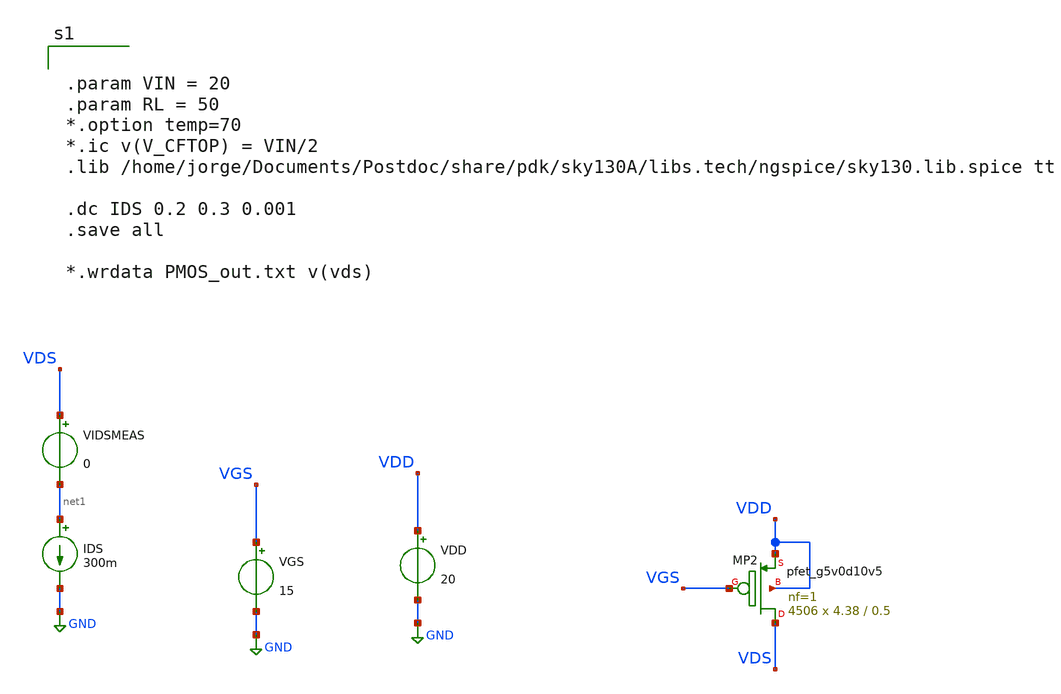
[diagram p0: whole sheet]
** sch_path: xschem/dev_switches/PMOS_allfingers_RONcalc_v2p1_20220623.sch
**.subckt PMOS_allfingers_RONcalc_v2p1_20220623
VGS VGS GND 15
IDS net1 GND 300m
VIDSMEAS VDS net1 0
XMP2 VDS VGS VDD VDD sky130_fd_pr__pfet_g5v0d10v5 L=0.5 W=4.38 nf=1 ad='int((nf+1)/2) * W/nf * 0.29'
+ as='int((nf+2)/2) * W/nf * 0.29' pd='2*int((nf+1)/2) * (W/nf + 0.29)' ps='2*int((nf+2)/2) * (W/nf + 0.29)'
+ nrd='0.29 / W' nrs='0.29 / W' sa=0 sb=0 sd=0 mult=4506 m=4506
VDD VDD GND 20
**** begin user architecture code


.param VIN = 20
.param RL = 50
*.option temp=70
*.ic v(V_CFTOP) = VIN/2
.lib /home/jorge/Documents/Postdoc/share/pdk/sky130A/libs.tech/ngspice/sky130.lib.spice tt

.dc IDS 0.2 0.3 0.001
.save all

*.wrdata PMOS_out.txt v(vds)


**** end user architecture code
**.ends
.GLOBAL GND
.end
